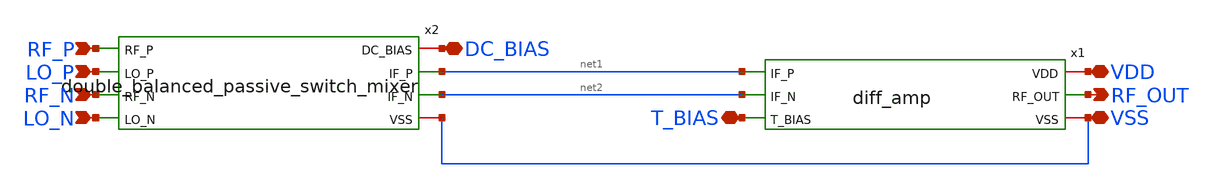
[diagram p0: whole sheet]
** sch_path: member_project/MIXER/noritsuna/xschem/double_balanced_passive_switch_mixer_w_amp.sch
**.subckt double_balanced_passive_switch_mixer_w_amp T_BIAS RF_OUT RF_P LO_P RF_N LO_N DC_BIAS VDD
*+ VSS
*.iopin T_BIAS
*.opin RF_OUT
*.ipin RF_P
*.ipin LO_P
*.ipin RF_N
*.ipin LO_N
*.iopin DC_BIAS
*.iopin VDD
*.iopin VSS
x1 VDD RF_OUT net1 net2 T_BIAS VSS diff_amp
x2 DC_BIAS RF_P LO_P RF_N LO_N net1 net2 VSS double_balanced_passive_switch_mixer
**.ends

* expanding   symbol:  diff_amp.sym # of pins=6
** sym_path: member_project/MIXER/noritsuna/xschem/diff_amp.sym
** sch_path: member_project/MIXER/noritsuna/xschem/diff_amp.sch
.subckt diff_amp VDD RF_OUT IF_P IF_N T_BIAS VSS
*.ipin IF_P
*.ipin IF_N
*.ipin T_BIAS
*.iopin VDD
*.iopin VSS
*.opin RF_OUT
XXM1 DM_P_1 DM_P_1 VDD VDD PMOS w=50u l=2u nrd=0 nrs=0 m=1
XXM2 RF_OUT DM_P_1 VDD VDD PMOS w=50u l=2u nrd=0 nrs=0 m=1
XXM3 DM_P_1 IF_P DM_N_3 VSS NMOS w=50u l=1u nrd=0 nrs=0 m=1
XXM4 RF_OUT IF_N DM_N_3 VSS NMOS w=50u l=1u nrd=0 nrs=0 m=1
XXM5 DM_N_3 T_BIAS VSS VSS NMOS w=100u l=1u nrd=0 nrs=0 m=1
XXC2 RF_OUT VSS VSS F_CSIO c=960f x=40u y=40u m=4
XXM6 DM_P_1 VDD VDD VDD PMOS w=5u l=2u nrd=0 nrs=0 m=2
XXM7 RF_OUT VDD VDD VDD PMOS w=5u l=2u nrd=0 nrs=0 m=2
XXM8 DM_P_1 VSS VSS VSS NMOS w=5u l=1u nrd=0 nrs=0 m=2
XXM11 VSS VSS VSS VSS NMOS w=5u l=1u nrd=0 nrs=0 m=4
XXM9 RF_OUT VSS VSS VSS NMOS w=5u l=1u nrd=0 nrs=0 m=2
.ends


* expanding   symbol:  double_balanced_passive_switch_mixer.sym # of pins=8
** sym_path: member_project/MIXER/noritsuna/xschem/double_balanced_passive_switch_mixer.sym
** sch_path: member_project/MIXER/noritsuna/xschem/double_balanced_passive_switch_mixer.sch
.subckt double_balanced_passive_switch_mixer DC_BIAS RF_P LO_P RF_N LO_N IF_P IF_N VSS
*.iopin DC_BIAS
*.ipin RF_P
*.ipin LO_P
*.ipin RF_N
*.ipin LO_N
*.opin IF_N
*.opin IF_P
*.iopin VSS
XXM1 RF_P LO_P IF_P VSS NMOS w=100u l=1u nrd=0 nrs=0 m=1
XXM2 RF_P LO_N IF_N VSS NMOS w=100u l=1u nrd=0 nrs=0 m=1
XXM3 RF_N LO_N IF_P VSS NMOS w=100u l=1u nrd=0 nrs=0 m=1
XXM4 RF_N LO_P IF_N VSS NMOS w=100u l=1u nrd=0 nrs=0 m=1
XR1 DC_BIAS RF_P DC_BIAS F_RR w=2.8e-06 l=49.4e-06 R=20.0e+03 tc1=0 tc2=0 m=1
XR2 DC_BIAS IF_P DC_BIAS F_RR w=2.8e-06 l=49.4e-06 R=20.0e+03 tc1=0 tc2=0 m=1
XXC1 IF_P VSS VSS F_CSIO c=4.86p x=90u y=90u m=4
XXC2 IF_N VSS VSS F_CSIO c=4.86p x=90u y=90u m=4
XR3 DC_BIAS IF_N DC_BIAS F_RR w=2.8e-06 l=49.4e-06 R=20.0e+03 tc1=0 tc2=0 m=1
XXM6 IF_P VSS VSS VSS NMOS w=10u l=1u nrd=0 nrs=0 m=4
XXM7 IF_N VSS VSS VSS NMOS w=10u l=1u nrd=0 nrs=0 m=4
.ends

.end
